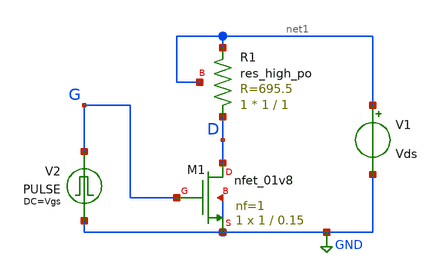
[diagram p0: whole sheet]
** sch_path: sky130A/xschem_libs/sky130_tests/test_nfet_TRAN/schematic/test_nfet_TRAN.sch
**.subckt test_nfet_TRAN
XM1 D G GND GND sky130_fd_pr__nfet_01v8 L=0.15 W=1 nf=1 ad='int((1 + 1)/2) * 1 / 1 * 0.29' as='int((1 + 2)/2) * 1 / 1 * 0.29'
+ pd='2*int((1 + 1)/2) * (1 / 1 + 0.29)' ps='2*int((1 + 2)/2) * (1 / 1 + 0.29)' nrd='0.29 / 1 ' nrs='0.29 / 1 '
+ sa=0 sb=0 sd=0 mult=1 m=1
V1 net1 GND Vds
V2 G GND Vgs PULSE(0 Vgs 10n 1n 1n 50n 100n )
XR1 D net1 net1 sky130_fd_pr__res_high_po W=1 L=1 mult=1 m=1
**.ends
.GLOBAL GND
.end
